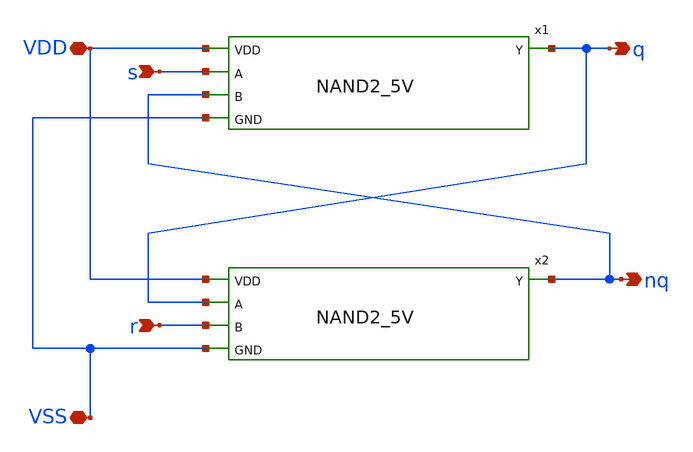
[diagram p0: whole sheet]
** sch_path: ADC/4bit_C2C/MagicAndSpice/SR_latch.sch
**.subckt SR_latch s r VDD VSS q nq
*.ipin s
*.ipin r
*.iopin VDD
*.iopin VSS
*.opin q
*.opin nq
x1 VDD q s nq VSS NAND2_5V
x2 VDD nq q r VSS NAND2_5V
**.ends

* expanding   symbol:  NAND2_5V.sym # of pins=5
** sym_path: ADC/16bit_C2C/MagicAndSpice/EE431_FinalProj/NAND2_5V.sym
** sch_path: ADC/16bit_C2C/MagicAndSpice/EE431_FinalProj/NAND2_5V.sch
.subckt NAND2_5V VDD Y A B GND
*.ipin A
*.ipin B
*.ipin VDD
*.ipin GND
*.opin Y
XM1 Y B VDD VDD sky130_fd_pr__pfet_g5v0d10v5 L=1 W=2 nf=1 ad='int((nf+1)/2) * W/nf * 0.29' as='int((nf+2)/2) * W/nf * 0.29'
+ pd='2*int((nf+1)/2) * (W/nf + 0.29)' ps='2*int((nf+2)/2) * (W/nf + 0.29)' nrd='0.29 / W' nrs='0.29 / W'
+ sa=0 sb=0 sd=0 mult=1 m=1
XM2 Y A VDD VDD sky130_fd_pr__pfet_g5v0d10v5 L=1 W=2 nf=1 ad='int((nf+1)/2) * W/nf * 0.29' as='int((nf+2)/2) * W/nf * 0.29'
+ pd='2*int((nf+1)/2) * (W/nf + 0.29)' ps='2*int((nf+2)/2) * (W/nf + 0.29)' nrd='0.29 / W' nrs='0.29 / W'
+ sa=0 sb=0 sd=0 mult=1 m=1
XM3 Y A net1 GND sky130_fd_pr__nfet_g5v0d10v5 L=1 W=2 nf=1 ad='int((nf+1)/2) * W/nf * 0.29' as='int((nf+2)/2) * W/nf * 0.29'
+ pd='2*int((nf+1)/2) * (W/nf + 0.29)' ps='2*int((nf+2)/2) * (W/nf + 0.29)' nrd='0.29 / W' nrs='0.29 / W'
+ sa=0 sb=0 sd=0 mult=1 m=1
XM4 net1 B GND GND sky130_fd_pr__nfet_g5v0d10v5 L=1 W=2 nf=1 ad='int((nf+1)/2) * W/nf * 0.29' as='int((nf+2)/2) * W/nf * 0.29'
+ pd='2*int((nf+1)/2) * (W/nf + 0.29)' ps='2*int((nf+2)/2) * (W/nf + 0.29)' nrd='0.29 / W' nrs='0.29 / W'
+ sa=0 sb=0 sd=0 mult=1 m=1
.ends

.end
